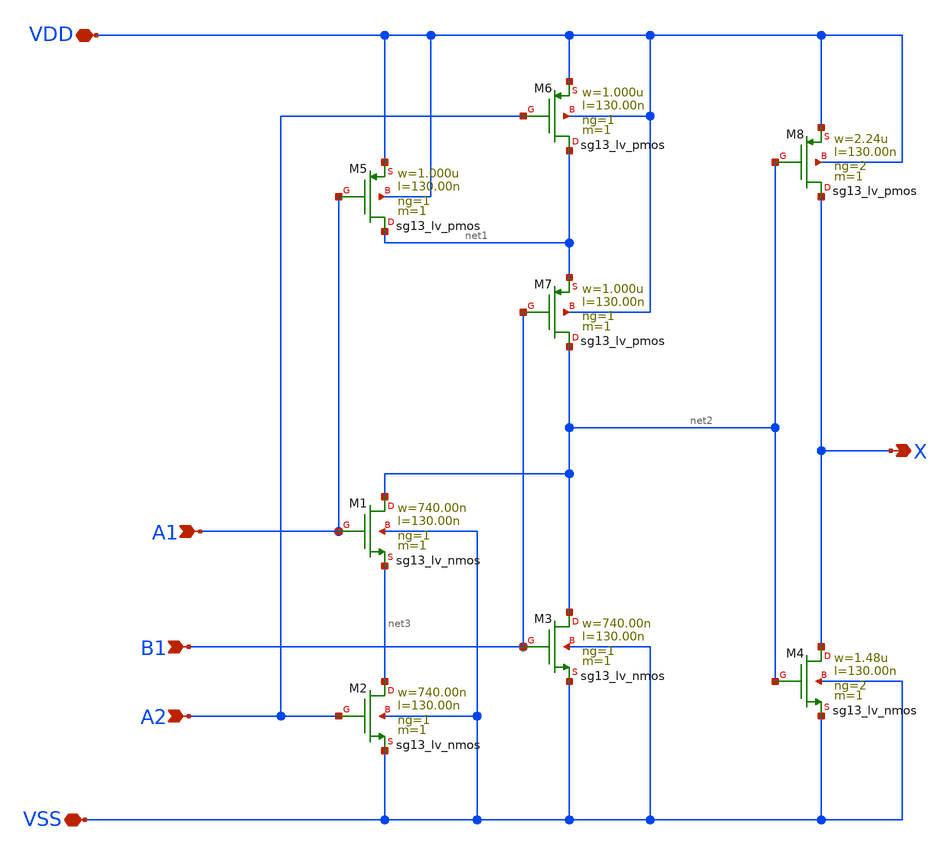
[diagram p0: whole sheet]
** sch_path: ihp-sg13g2/libs.tech/xschem/sg13g2_stdcells/sg13g2_a21o_2.sch
* Copyright 2023 IHP PDK Authors
* Licensed under the Apache License, Version 2.0 (the "License");
* you may not use this file except in compliance with the License.
* You may obtain a copy of the License at
* https://www.apache.org/licenses/LICENSE-2.0
* Unless required by applicable law or agreed to in writing, software
* distributed under the License is distributed on an "AS IS" BASIS,
* WITHOUT WARRANTIES OR CONDITIONS OF ANY KIND, either express or implied.
* See the License for the specific language governing permissions and
* limitations under the License.
**.subckt sg13g2_a21o_2 X A1 A2 B1 VDD VSS
*.opin X
*.ipin A1
*.ipin A2
*.ipin B1
*.iopin VDD
*.iopin VSS
XM1 net2 A1 net3 VSS sg13_lv_nmos w=740.00n l=130.00n ng=1 m=1 mm_ok=1
XM2 net3 A2 VSS VSS sg13_lv_nmos w=740.00n l=130.00n ng=1 m=1 mm_ok=1
XM3 net2 B1 VSS VSS sg13_lv_nmos w=740.00n l=130.00n ng=1 m=1 mm_ok=1
XM4 X net2 VSS VSS sg13_lv_nmos w=1.48u l=130.00n ng=2 m=1 mm_ok=1
XM5 net1 A1 VDD VDD sg13_lv_pmos w=1.000u l=130.00n ng=1 m=1 mm_ok=1
XM6 net1 A2 VDD VDD sg13_lv_pmos w=1.000u l=130.00n ng=1 m=1 mm_ok=1
XM7 net2 B1 net1 VDD sg13_lv_pmos w=1.000u l=130.00n ng=1 m=1 mm_ok=1
XM8 X net2 VDD VDD sg13_lv_pmos w=2.24u l=130.00n ng=2 m=1 mm_ok=1
**.ends
.end
